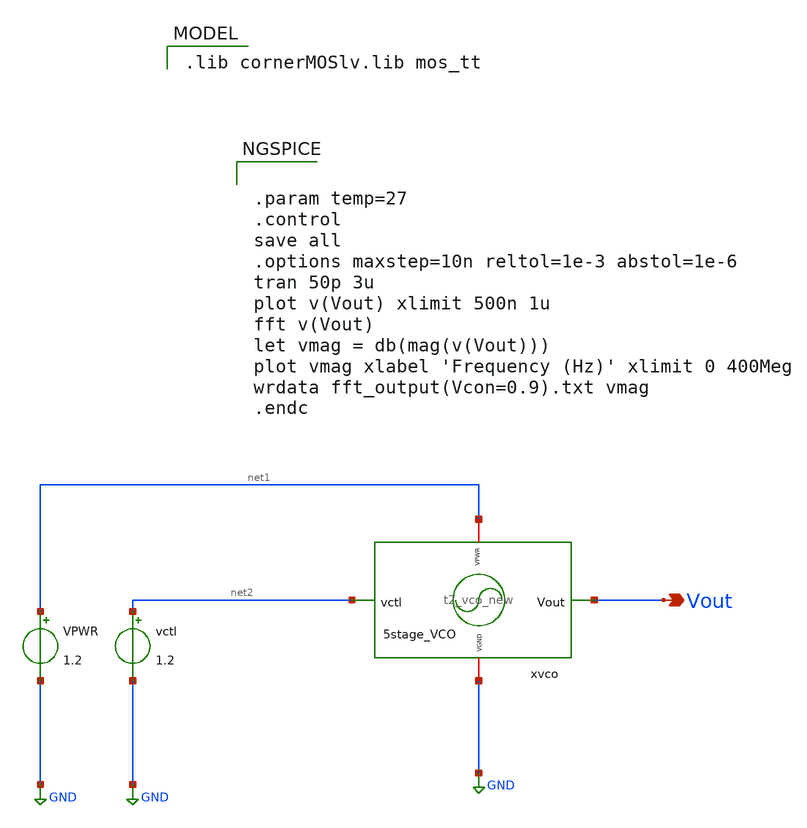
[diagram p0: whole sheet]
** sch_path: Team 2 Design/design_data/xschem/t2_vco_new_tb.sch
**.subckt t2_vco_new_tb Vout
*.opin Vout
x1 net1 GND net2 Vout t2_vco_new
VPWR net1 GND 1.2
vctl net2 GND 1.2
**** begin user architecture code
 .lib cornerMOSlv.lib mos_tt



.param temp=27
.control
save all
.options maxstep=10n reltol=1e-3 abstol=1e-6
tran 50p 3u
plot v(Vout) xlimit 500n 1u
fft v(Vout)
let vmag = db(mag(v(Vout)))
plot vmag xlabel 'Frequency (Hz)' xlimit 0 400Meg
wrdata fft_output(Vcon=0.9).txt vmag
.endc


**** end user architecture code
**.ends
.GLOBAL GND
.end
